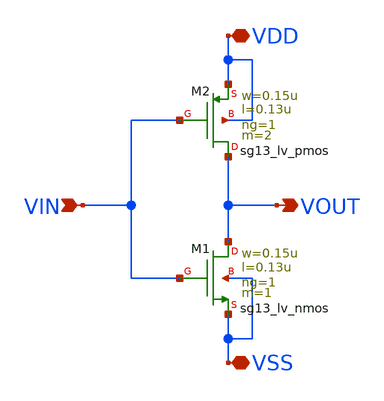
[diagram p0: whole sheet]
** sch_path: 4xPI/inv.sch
**.subckt inv VDD VSS VOUT VIN
*.iopin VDD
*.iopin VSS
*.opin VOUT
*.ipin VIN
XM2 VOUT VIN VDD VDD sg13_lv_pmos w=0.15u l=0.13u ng=1 m=2 mm_ok=1
XM1 VOUT VIN VSS VSS sg13_lv_nmos w=0.15u l=0.13u ng=1 m=1 mm_ok=1
**.ends
.end
